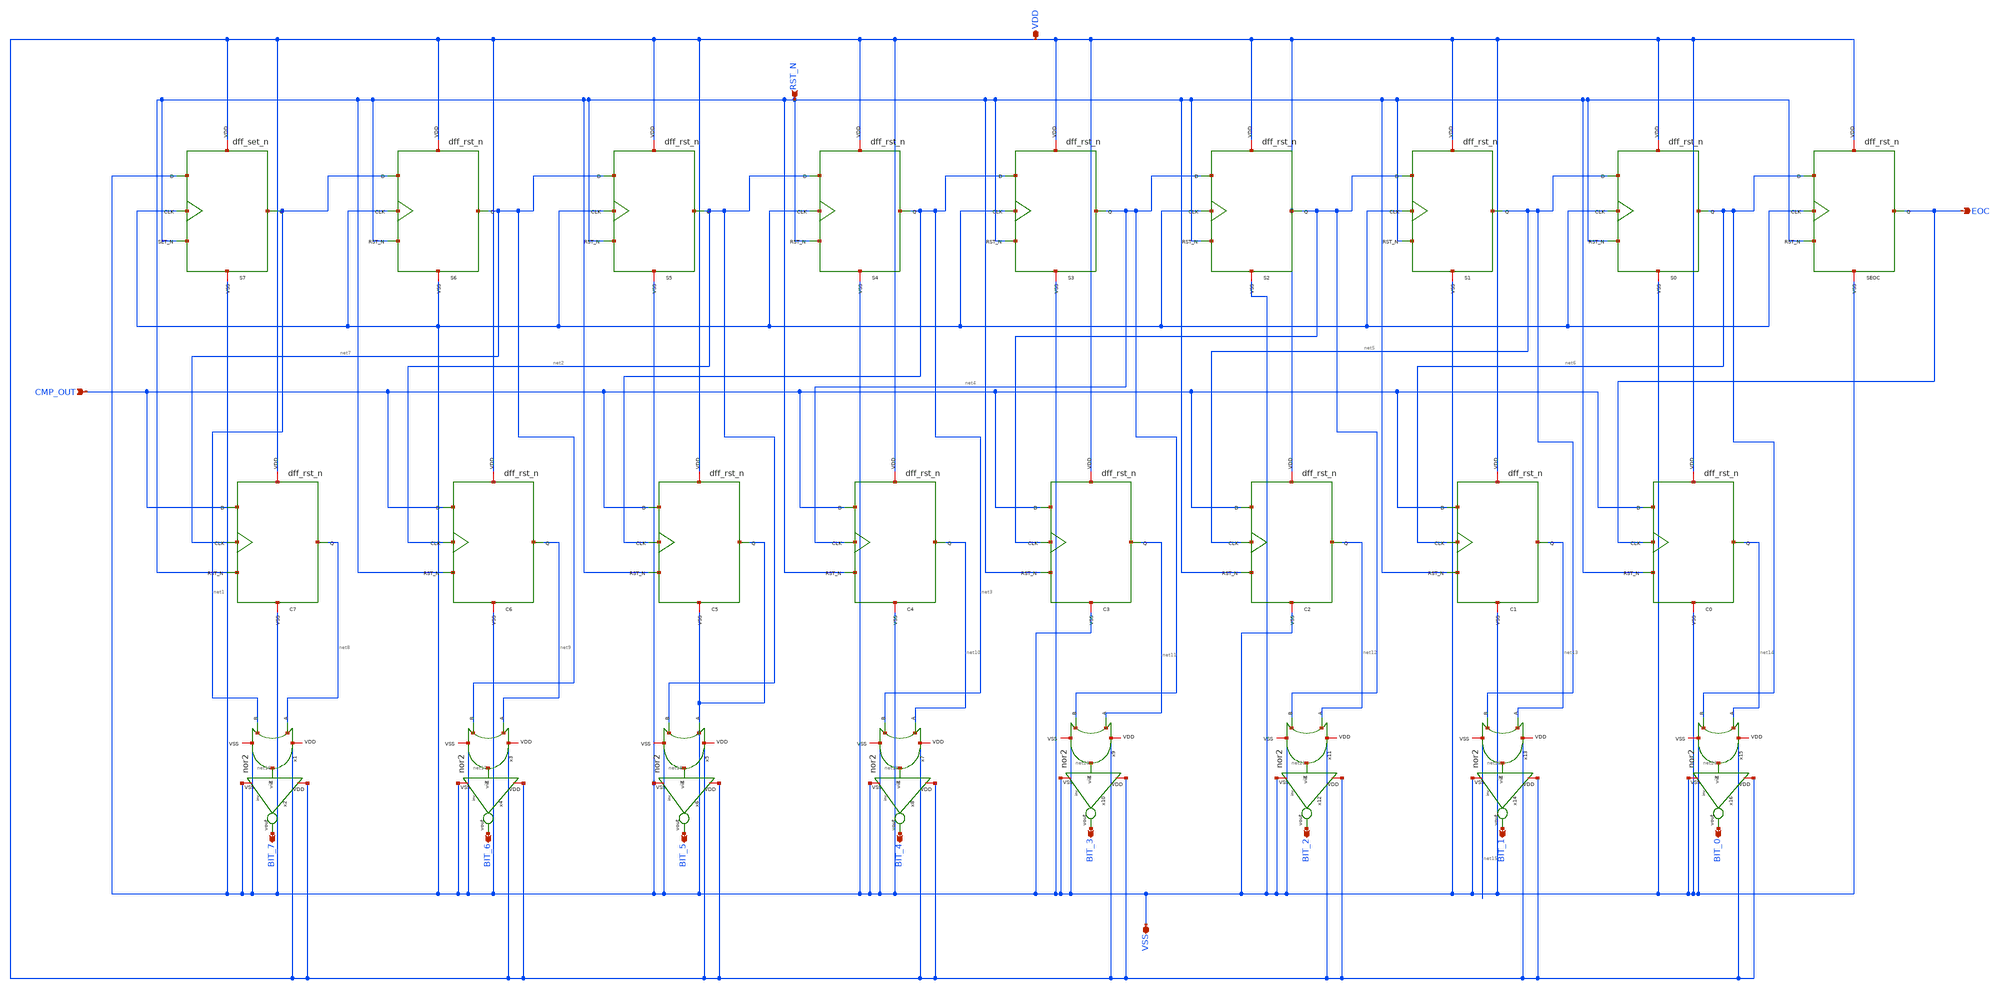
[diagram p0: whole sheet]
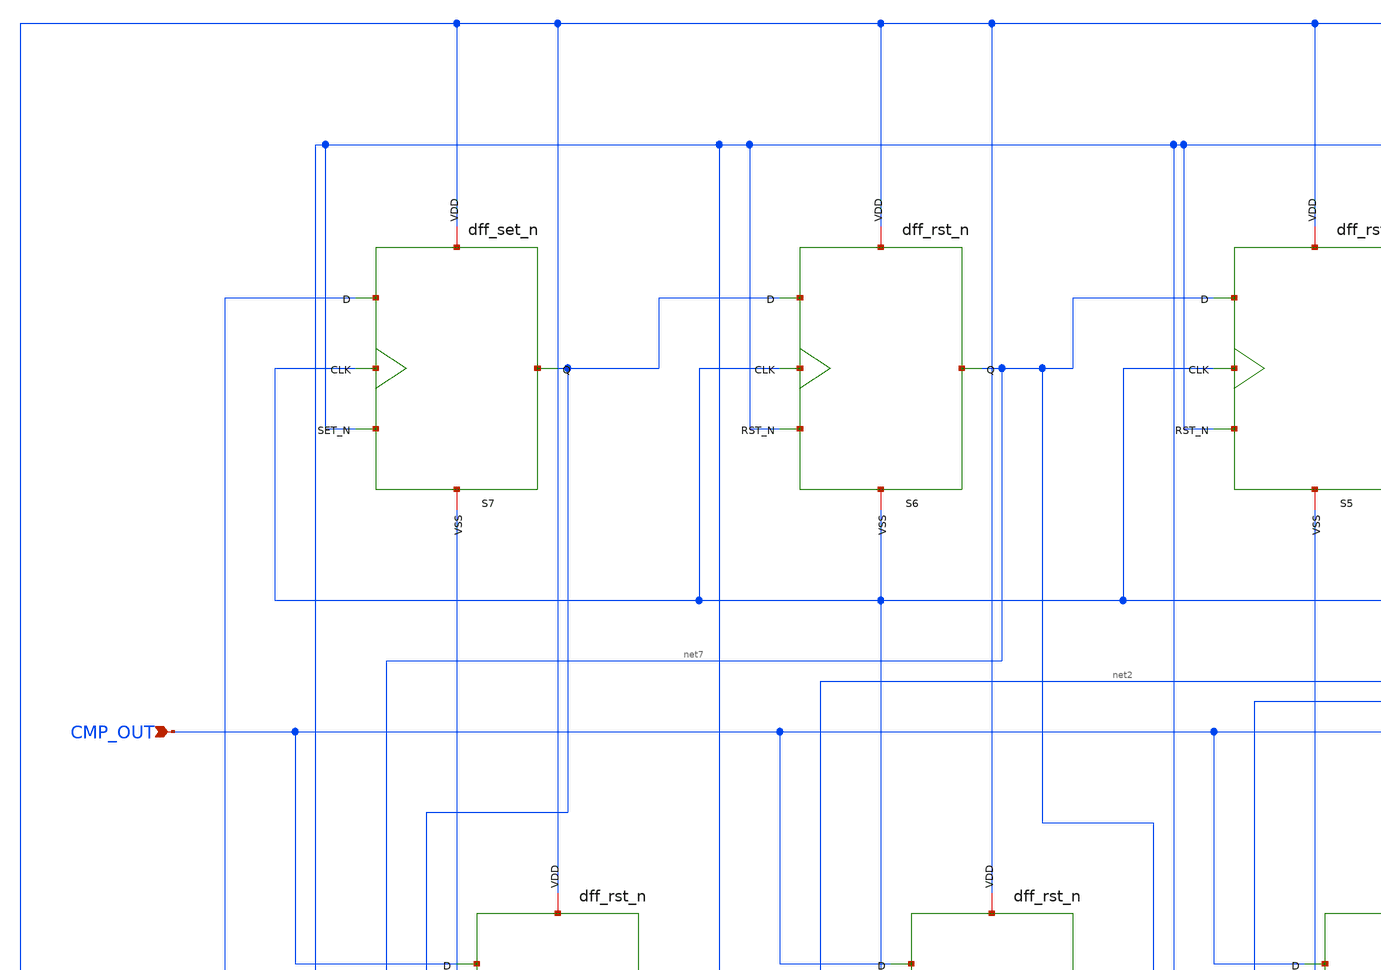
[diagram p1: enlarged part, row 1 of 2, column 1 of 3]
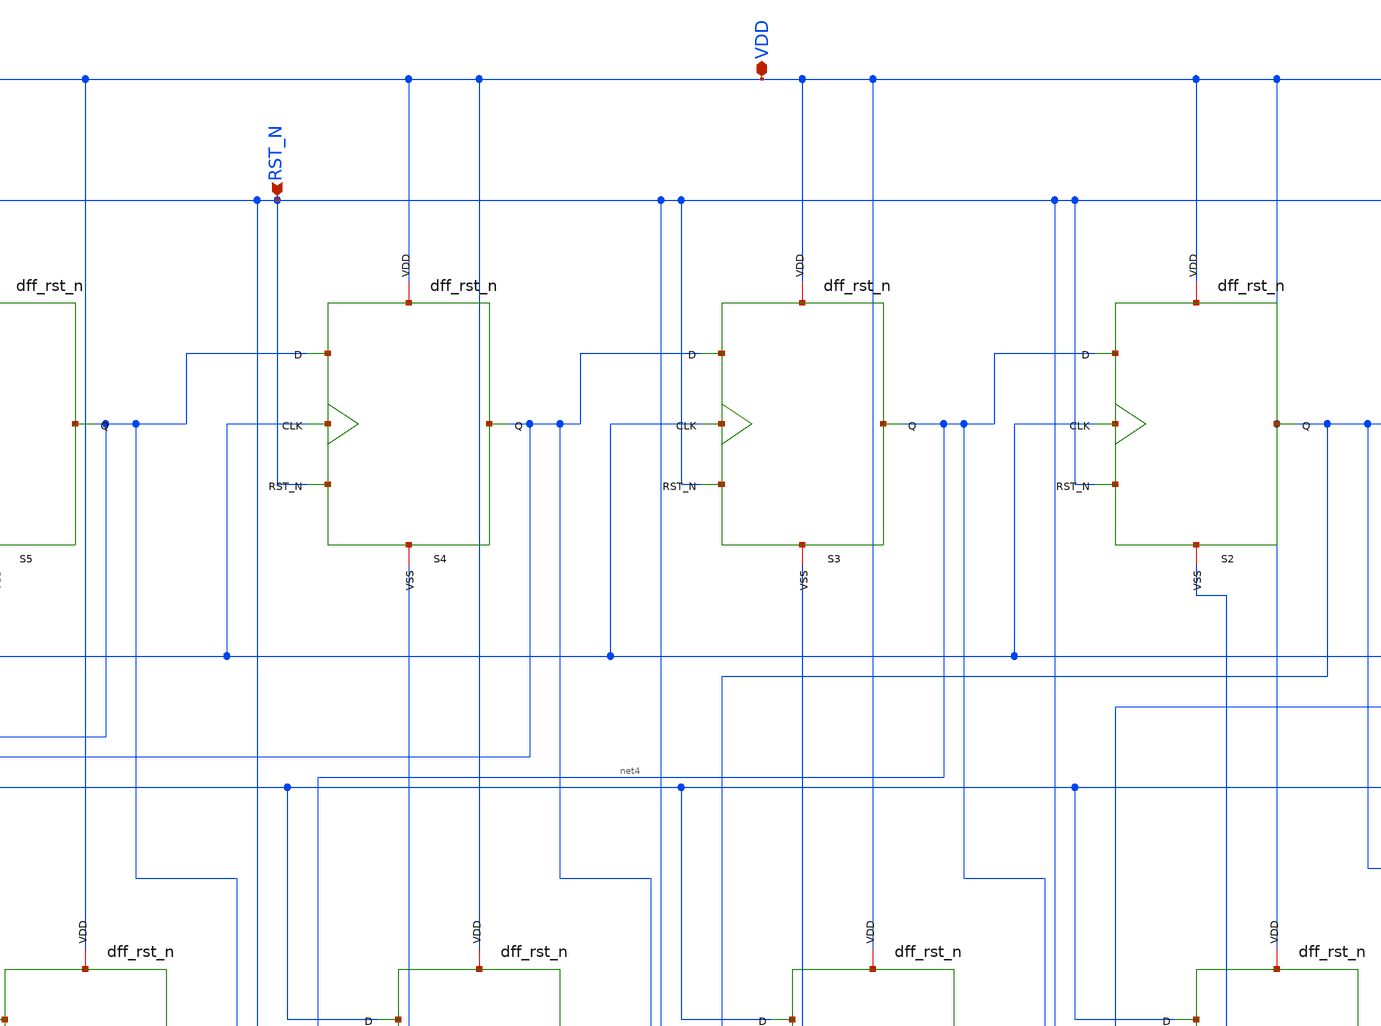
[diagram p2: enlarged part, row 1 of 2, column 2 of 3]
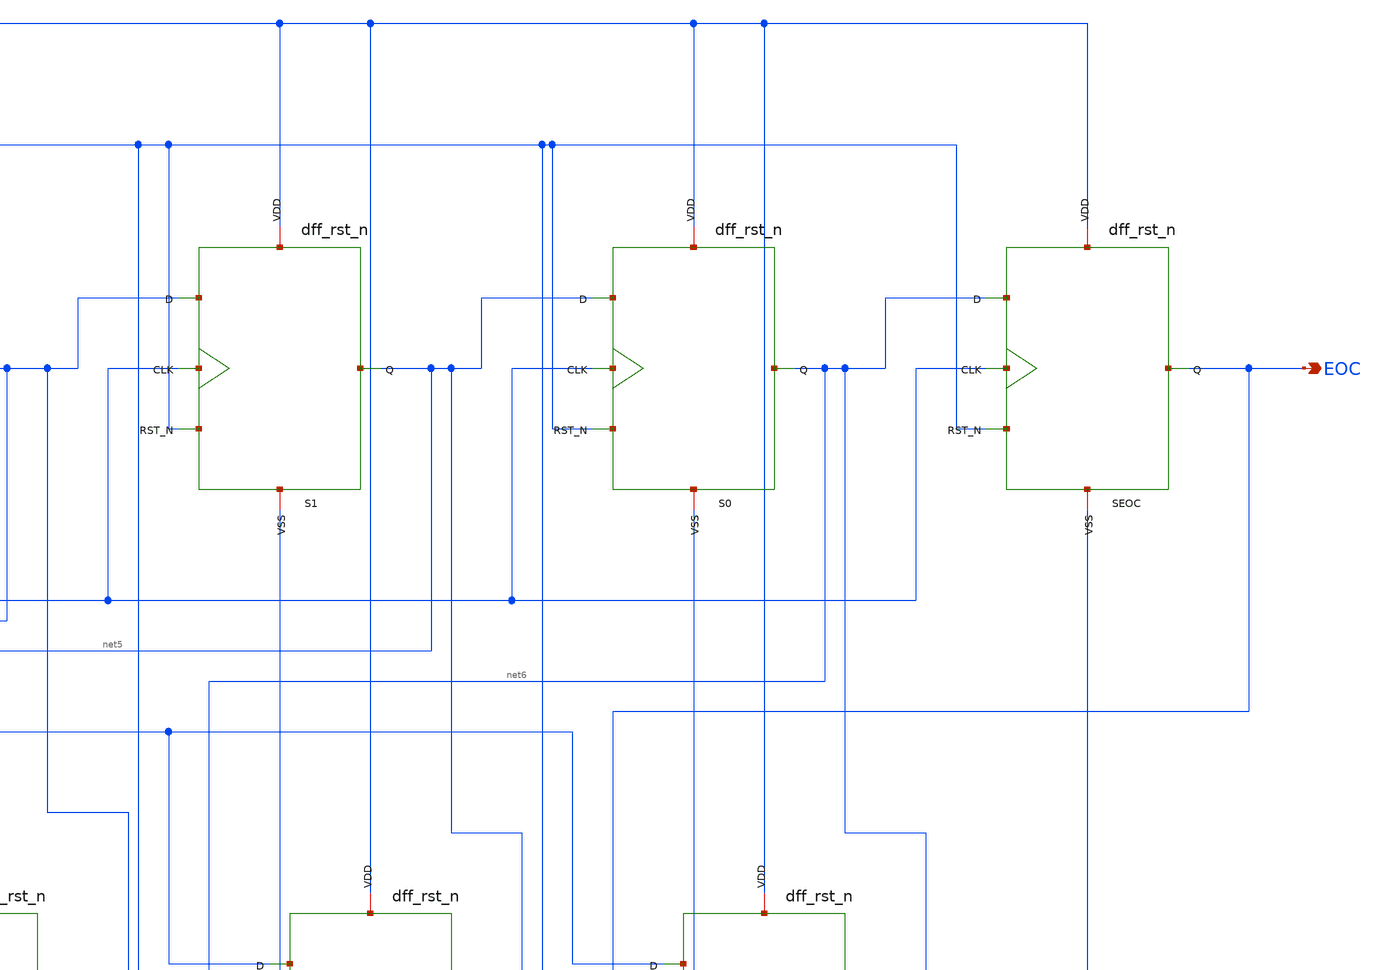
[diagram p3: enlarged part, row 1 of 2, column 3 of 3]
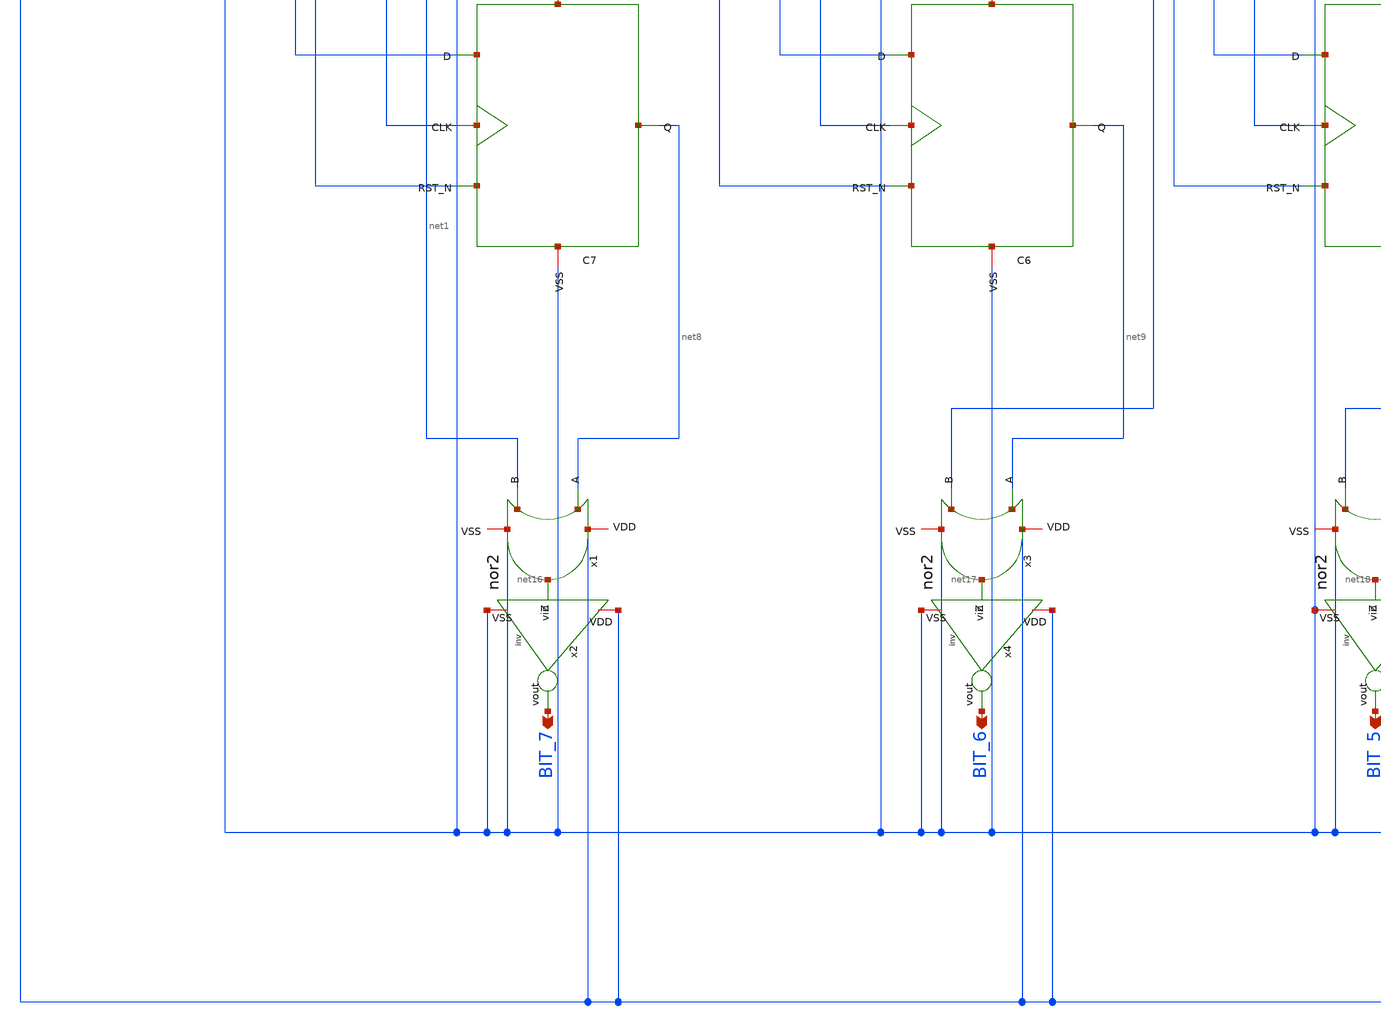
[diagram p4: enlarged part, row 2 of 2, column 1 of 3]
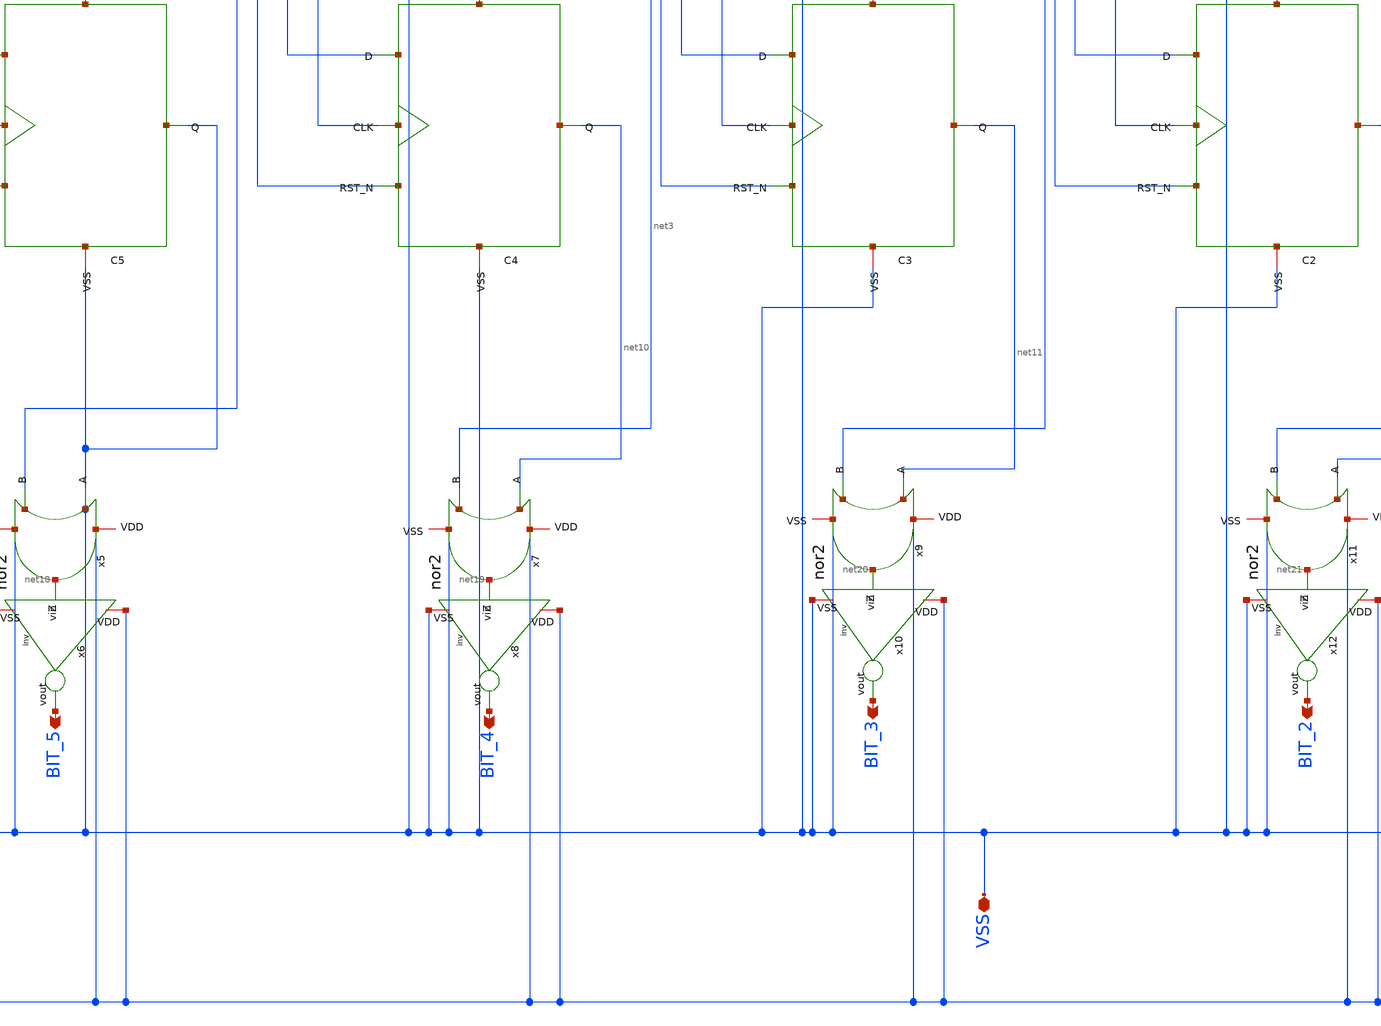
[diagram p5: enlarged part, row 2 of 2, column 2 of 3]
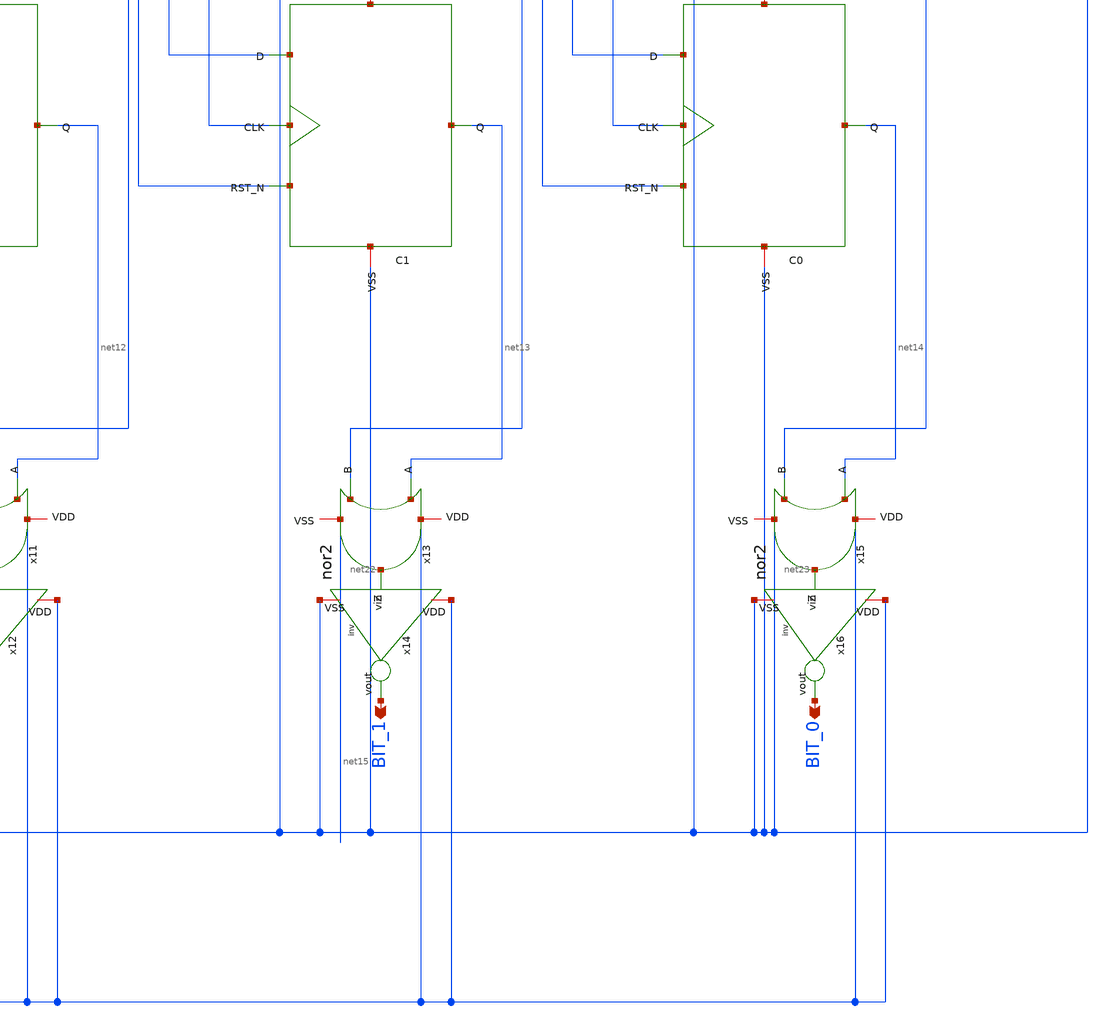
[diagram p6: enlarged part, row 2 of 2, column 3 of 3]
** sch_path: sar_logic/sar_designs/sar_logic.sch
**.subckt sar_logic VDD VSS BIT_7 BIT_6 BIT_5 BIT_4 BIT_3 BIT_2 BIT_1 BIT_0 EOC RST_N CMP_OUT
*.iopin VDD
*.iopin VSS
*.opin BIT_7
*.opin BIT_6
*.opin BIT_5
*.opin BIT_4
*.opin BIT_3
*.opin BIT_2
*.opin BIT_1
*.opin BIT_0
*.opin EOC
*.ipin RST_N
*.ipin CMP_OUT
S7 VDD VSS VSS net1 RST_N VSS dff_set_n
S6 VDD VSS net1 net7 RST_N VSS dff_rst_n
S5 VDD VSS net7 net2 RST_N VSS dff_rst_n
S4 VDD VSS net2 net3 RST_N VSS dff_rst_n
S3 VDD VSS net3 net4 RST_N VSS dff_rst_n
S2 VDD VSS net4 VDD RST_N VSS dff_rst_n
S1 VDD VSS VDD net5 RST_N VSS dff_rst_n
S0 VDD VSS net5 net6 RST_N VSS dff_rst_n
SEOC VDD VSS net6 EOC RST_N VSS dff_rst_n
C7 VDD net7 CMP_OUT net8 RST_N VSS dff_rst_n
C6 VDD net2 CMP_OUT net9 RST_N VSS dff_rst_n
C5 VDD net3 CMP_OUT VSS RST_N VSS dff_rst_n
C4 VDD net4 CMP_OUT net10 RST_N VSS dff_rst_n
C3 VDD VDD CMP_OUT net11 RST_N VSS dff_rst_n
C2 VDD net5 CMP_OUT net12 RST_N VSS dff_rst_n
C1 VDD net6 CMP_OUT net13 RST_N VSS dff_rst_n
C0 VDD EOC CMP_OUT net14 RST_N VSS dff_rst_n
x1 VDD net8 net1 net16 VSS nor2
x2 VDD net16 BIT_7 VSS inv
x3 VDD net9 net7 net17 VSS nor2
x4 VDD net17 BIT_6 VSS inv
x5 VDD VSS net2 net18 VSS nor2
x6 VDD net18 BIT_5 VSS inv
x7 VDD net10 net3 net19 VSS nor2
x8 VDD net19 BIT_4 VSS inv
x9 VDD net11 net4 net20 VSS nor2
x10 VDD net20 BIT_3 VSS inv
x11 VDD net12 VDD net21 VSS nor2
x12 VDD net21 BIT_2 VSS inv
x13 VDD net13 net5 net22 net15 nor2
x14 VDD net22 BIT_1 VSS inv
x15 VDD net14 net6 net23 VSS nor2
x16 VDD net23 BIT_0 VSS inv
**.ends
.end
